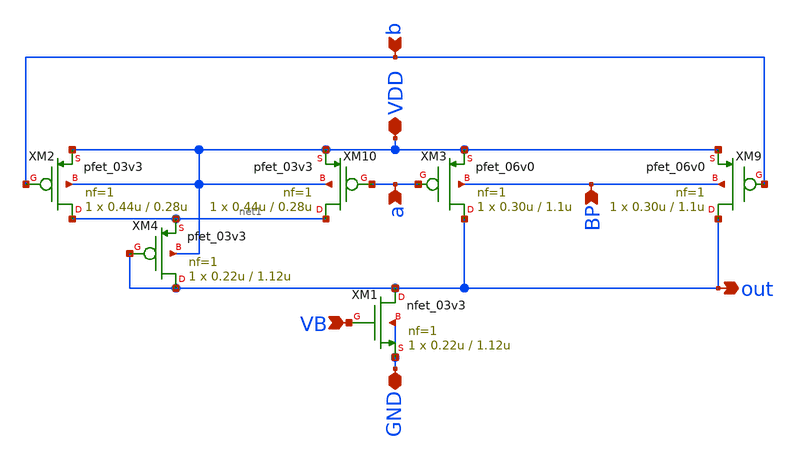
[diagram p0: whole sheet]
** sch_path: xschem_designs/NMIN_P.sch
**.subckt NMIN_P a out GND VDD BP VB b
*.ipin a
*.opin out
*.iopin GND
*.iopin VDD
*.ipin BP
*.ipin VB
*.ipin b
XM1 out VB GND GND nfet_03v3 L=1.12u W=0.22u nf=1 ad='int((nf+1)/2) * W/nf * 0.18u' as='int((nf+2)/2) * W/nf * 0.18u'
+ pd='2*int((nf+1)/2) * (W/nf + 0.18u)' ps='2*int((nf+2)/2) * (W/nf + 0.18u)' nrd='0.18u / W' nrs='0.18u / W'
+ sa=0 sb=0 sd=0 m=1 par=1
XM2 net1 b VDD VDD pfet_03v3 L=0.28u W=0.44u nf=1 ad='int((nf+1)/2) * W/nf * 0.18u' as='int((nf+2)/2) * W/nf * 0.18u'
+ pd='2*int((nf+1)/2) * (W/nf + 0.18u)' ps='2*int((nf+2)/2) * (W/nf + 0.18u)' nrd='0.18u / W' nrs='0.18u / W'
+ sa=0 sb=0 sd=0 m=1 par=1
XM3 out a VDD BP pfet_06v0 L=1.1u W=0.30u nf=1 ad='int((nf+1)/2) * W/nf * 0.18u' as='int((nf+2)/2) * W/nf * 0.18u'
+ pd='2*int((nf+1)/2) * (W/nf + 0.18u)' ps='2*int((nf+2)/2) * (W/nf + 0.18u)' nrd='0.18u / W' nrs='0.18u / W'
+ sa=0 sb=0 sd=0 m=1
XM4 out out net1 VDD pfet_03v3 L=1.12u W=0.22u nf=1 ad='int((nf+1)/2) * W/nf * 0.18u' as='int((nf+2)/2) * W/nf * 0.18u'
+ pd='2*int((nf+1)/2) * (W/nf + 0.18u)' ps='2*int((nf+2)/2) * (W/nf + 0.18u)' nrd='0.18u / W' nrs='0.18u / W'
+ sa=0 sb=0 sd=0 m=1 par=1
XM9 out b VDD BP pfet_06v0 L=1.1u W=0.30u nf=1 ad='int((nf+1)/2) * W/nf * 0.18u' as='int((nf+2)/2) * W/nf * 0.18u'
+ pd='2*int((nf+1)/2) * (W/nf + 0.18u)' ps='2*int((nf+2)/2) * (W/nf + 0.18u)' nrd='0.18u / W' nrs='0.18u / W'
+ sa=0 sb=0 sd=0 m=1
XM10 net1 a VDD VDD pfet_03v3 L=0.28u W=0.44u nf=1 ad='int((nf+1)/2) * W/nf * 0.18u' as='int((nf+2)/2) * W/nf * 0.18u'
+ pd='2*int((nf+1)/2) * (W/nf + 0.18u)' ps='2*int((nf+2)/2) * (W/nf + 0.18u)' nrd='0.18u / W' nrs='0.18u / W'
+ sa=0 sb=0 sd=0 m=1 par=1
**.ends
.end
